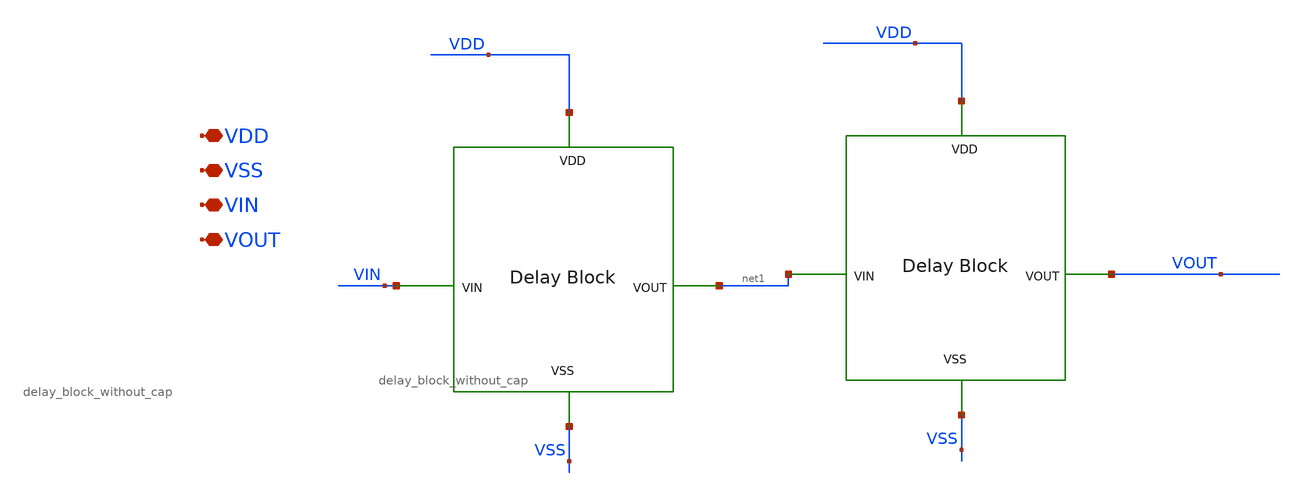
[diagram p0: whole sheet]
** sch_path: xschem/DC_DC_Converter_xschem/OTHERS/DC_DC_Converter_JV8/Delay_block_revised/delay_block_stage2.sch
**.subckt delay_block_stage2 VDD VSS VIN VOUT
*.iopin VDD
*.iopin VSS
*.iopin VIN
*.iopin VOUT
x1 net1 VIN VDD VSS delay_block_without_cap
x2 VOUT net1 VDD VSS delay_block_without_cap
**.ends
.end
